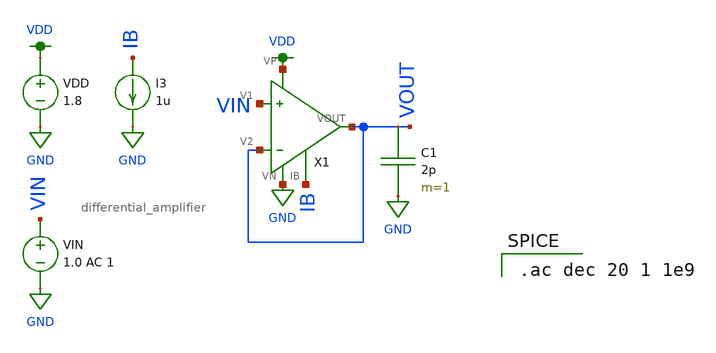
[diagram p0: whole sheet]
** sch_path: mp3/schematics/differential_amplifier_tran_d.sch
**.subckt differential_amplifier_tran_d
VDD VDD GND 1.8
VIN VIN GND 1.0 AC 1
C1 VOUT GND 2p m=1
X1 VIN VOUT VDD GND IB VOUT differential_amplifier
I3 IB GND 1u
**** begin user architecture code

.option wnflag=1
.lib ~/skywater/skywater-pdk/libraries/sky130_fd_pr_ngspice/latest/models/sky130.lib.spice tt


.ac dec 20 1 1e9

**** end user architecture code
**.ends
.GLOBAL GND
.GLOBAL VDD
.end
